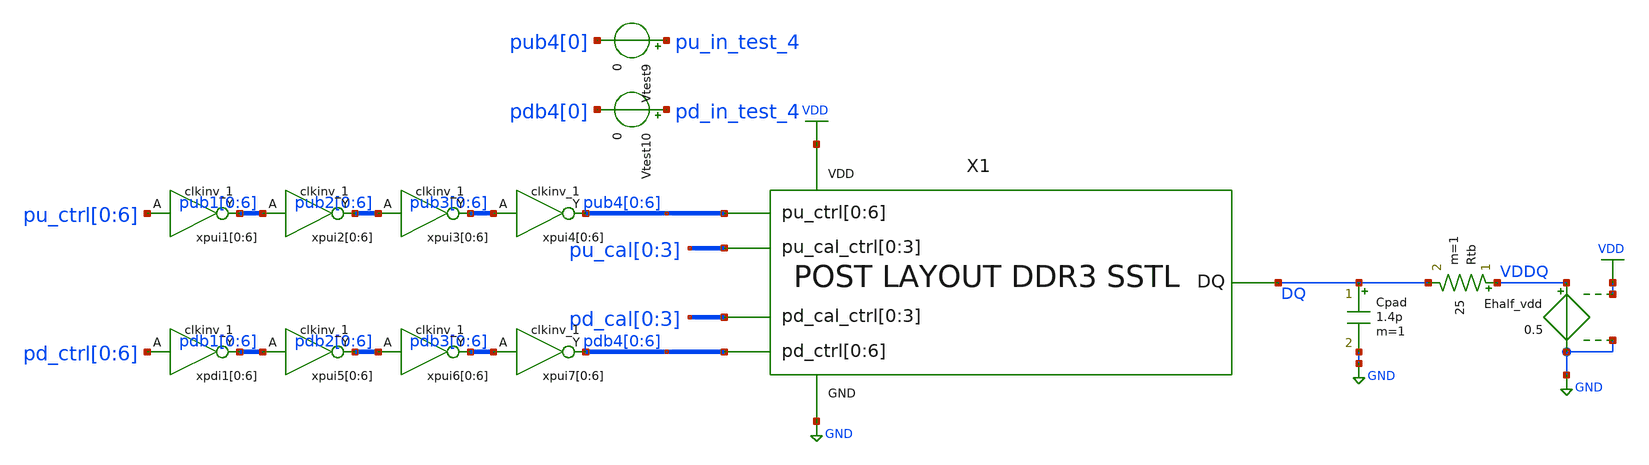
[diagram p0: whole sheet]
** sch_path: schem/post_layout_sstl_slew_tb.sch
* Copyright 2021 Stefan Frederik Schippers
* Licensed under the Apache License, Version 2.0 (the "License");
* you may not use this file except in compliance with the License.
* You may obtain a copy of the License at
* https://www.apache.org/licenses/LICENSE-2.0
* Unless required by applicable law or agreed to in writing, software
* distributed under the License is distributed on an "AS IS" BASIS,
* WITHOUT WARRANTIES OR CONDITIONS OF ANY KIND, either express or implied.
* See the License for the specific language governing permissions and
* limitations under the License.
**.subckt post_layout_sstl_slew_tb
Rtb VDDQ DQ 25 m=1
Cpad DQ GND 1.4p m=1
Ehalf_vdd VDDQ GND VDD GND 0.5
xpui1[0] pu_ctrl[0] GND GND VDD VDD pub1[0] sky130_fd_sc_hd__clkinv_1
xpui1[1] pu_ctrl[1] GND GND VDD VDD pub1[1] sky130_fd_sc_hd__clkinv_1
xpui1[2] pu_ctrl[2] GND GND VDD VDD pub1[2] sky130_fd_sc_hd__clkinv_1
xpui1[3] pu_ctrl[3] GND GND VDD VDD pub1[3] sky130_fd_sc_hd__clkinv_1
xpui1[4] pu_ctrl[4] GND GND VDD VDD pub1[4] sky130_fd_sc_hd__clkinv_1
xpui1[5] pu_ctrl[5] GND GND VDD VDD pub1[5] sky130_fd_sc_hd__clkinv_1
xpui1[6] pu_ctrl[6] GND GND VDD VDD pub1[6] sky130_fd_sc_hd__clkinv_1
xpdi1[0] pd_ctrl[0] GND GND VDD VDD pdb1[0] sky130_fd_sc_hd__clkinv_1
xpdi1[1] pd_ctrl[1] GND GND VDD VDD pdb1[1] sky130_fd_sc_hd__clkinv_1
xpdi1[2] pd_ctrl[2] GND GND VDD VDD pdb1[2] sky130_fd_sc_hd__clkinv_1
xpdi1[3] pd_ctrl[3] GND GND VDD VDD pdb1[3] sky130_fd_sc_hd__clkinv_1
xpdi1[4] pd_ctrl[4] GND GND VDD VDD pdb1[4] sky130_fd_sc_hd__clkinv_1
xpdi1[5] pd_ctrl[5] GND GND VDD VDD pdb1[5] sky130_fd_sc_hd__clkinv_1
xpdi1[6] pd_ctrl[6] GND GND VDD VDD pdb1[6] sky130_fd_sc_hd__clkinv_1
Vtest9 pu_in_test_4 pub4[0] 0
Vtest10 pd_in_test_4 pdb4[0] 0
xpui2[0] pub1[0] GND GND VDD VDD pub2[0] sky130_fd_sc_hd__clkinv_1
xpui2[1] pub1[1] GND GND VDD VDD pub2[1] sky130_fd_sc_hd__clkinv_1
xpui2[2] pub1[2] GND GND VDD VDD pub2[2] sky130_fd_sc_hd__clkinv_1
xpui2[3] pub1[3] GND GND VDD VDD pub2[3] sky130_fd_sc_hd__clkinv_1
xpui2[4] pub1[4] GND GND VDD VDD pub2[4] sky130_fd_sc_hd__clkinv_1
xpui2[5] pub1[5] GND GND VDD VDD pub2[5] sky130_fd_sc_hd__clkinv_1
xpui2[6] pub1[6] GND GND VDD VDD pub2[6] sky130_fd_sc_hd__clkinv_1
xpui3[0] pub2[0] GND GND VDD VDD pub3[0] sky130_fd_sc_hd__clkinv_1
xpui3[1] pub2[1] GND GND VDD VDD pub3[1] sky130_fd_sc_hd__clkinv_1
xpui3[2] pub2[2] GND GND VDD VDD pub3[2] sky130_fd_sc_hd__clkinv_1
xpui3[3] pub2[3] GND GND VDD VDD pub3[3] sky130_fd_sc_hd__clkinv_1
xpui3[4] pub2[4] GND GND VDD VDD pub3[4] sky130_fd_sc_hd__clkinv_1
xpui3[5] pub2[5] GND GND VDD VDD pub3[5] sky130_fd_sc_hd__clkinv_1
xpui3[6] pub2[6] GND GND VDD VDD pub3[6] sky130_fd_sc_hd__clkinv_1
xpui4[0] pub3[0] GND GND VDD VDD pub4[0] sky130_fd_sc_hd__clkinv_1
xpui4[1] pub3[1] GND GND VDD VDD pub4[1] sky130_fd_sc_hd__clkinv_1
xpui4[2] pub3[2] GND GND VDD VDD pub4[2] sky130_fd_sc_hd__clkinv_1
xpui4[3] pub3[3] GND GND VDD VDD pub4[3] sky130_fd_sc_hd__clkinv_1
xpui4[4] pub3[4] GND GND VDD VDD pub4[4] sky130_fd_sc_hd__clkinv_1
xpui4[5] pub3[5] GND GND VDD VDD pub4[5] sky130_fd_sc_hd__clkinv_1
xpui4[6] pub3[6] GND GND VDD VDD pub4[6] sky130_fd_sc_hd__clkinv_1
xpui5[0] pdb1[0] GND GND VDD VDD pdb2[0] sky130_fd_sc_hd__clkinv_1
xpui5[1] pdb1[1] GND GND VDD VDD pdb2[1] sky130_fd_sc_hd__clkinv_1
xpui5[2] pdb1[2] GND GND VDD VDD pdb2[2] sky130_fd_sc_hd__clkinv_1
xpui5[3] pdb1[3] GND GND VDD VDD pdb2[3] sky130_fd_sc_hd__clkinv_1
xpui5[4] pdb1[4] GND GND VDD VDD pdb2[4] sky130_fd_sc_hd__clkinv_1
xpui5[5] pdb1[5] GND GND VDD VDD pdb2[5] sky130_fd_sc_hd__clkinv_1
xpui5[6] pdb1[6] GND GND VDD VDD pdb2[6] sky130_fd_sc_hd__clkinv_1
xpui6[0] pdb2[0] GND GND VDD VDD pdb3[0] sky130_fd_sc_hd__clkinv_1
xpui6[1] pdb2[1] GND GND VDD VDD pdb3[1] sky130_fd_sc_hd__clkinv_1
xpui6[2] pdb2[2] GND GND VDD VDD pdb3[2] sky130_fd_sc_hd__clkinv_1
xpui6[3] pdb2[3] GND GND VDD VDD pdb3[3] sky130_fd_sc_hd__clkinv_1
xpui6[4] pdb2[4] GND GND VDD VDD pdb3[4] sky130_fd_sc_hd__clkinv_1
xpui6[5] pdb2[5] GND GND VDD VDD pdb3[5] sky130_fd_sc_hd__clkinv_1
xpui6[6] pdb2[6] GND GND VDD VDD pdb3[6] sky130_fd_sc_hd__clkinv_1
xpui7[0] pdb3[0] GND GND VDD VDD pdb4[0] sky130_fd_sc_hd__clkinv_1
xpui7[1] pdb3[1] GND GND VDD VDD pdb4[1] sky130_fd_sc_hd__clkinv_1
xpui7[2] pdb3[2] GND GND VDD VDD pdb4[2] sky130_fd_sc_hd__clkinv_1
xpui7[3] pdb3[3] GND GND VDD VDD pdb4[3] sky130_fd_sc_hd__clkinv_1
xpui7[4] pdb3[4] GND GND VDD VDD pdb4[4] sky130_fd_sc_hd__clkinv_1
xpui7[5] pdb3[5] GND GND VDD VDD pdb4[5] sky130_fd_sc_hd__clkinv_1
xpui7[6] pdb3[6] GND GND VDD VDD pdb4[6] sky130_fd_sc_hd__clkinv_1
X1 DQ GND pd_cal[0] pd_cal[1] pd_cal[2] pd_cal[3] pdb4[0] pdb4[1] pdb4[2] pdb4[3] pdb4[4] pdb4[5]
+ pdb4[6] pu_cal[0] pu_cal[1] pu_cal[2] pu_cal[3] pub4[0] pub4[1] pub4[2] pub4[3] pub4[4] pub4[5] pub4[6] VDD
+ SSTL
**** begin user architecture code
 ** Local library links to pdk
.lib ./sky130/libs/SED_process_SED_lib.spice SED_process_SED
.include $::SKYWATER_STDCELLS/sky130_fd_sc_hd.spice
.include ./layout/pex_SSTL.spice

**** end user architecture code
**.ends
.GLOBAL GND
.GLOBAL VDD
**** begin user architecture code


* power voltage
vvdd VDD 0 SED_vdd_SED

** CALIBRATION CONTROL **
* PULLUP
vpu_cal0 pu_cal[0] 0 SED_pucal0_SED
vpu_cal1 pu_cal[1] 0 SED_pucal1_SED
vpu_cal2 pu_cal[2] 0 SED_pucal2_SED
vpu_cal3 pu_cal[3] 0 SED_pucal3_SED
* PULLDOWN
vpd_cal0 pd_cal[0] 0 SED_pdcal0_SED
vpd_cal1 pd_cal[1] 0 SED_pdcal1_SED
vpd_cal2 pd_cal[2] 0 SED_pdcal2_SED
vpd_cal3 pd_cal[3] 0 SED_pdcal3_SED

** LEG ENABLE/DISABLE CONTROL
* PULLUP
*          vlow, vhigh, delay, risetime, falltime, pulsewidth, period, phase
vpu_ctrl0 pu_ctrl[0] 0 0 PULSE 0   SED_puctrl0_SED 1n 10p 10p 5n 10n 0
vpu_ctrl1 pu_ctrl[1] 0 0 PULSE 0   SED_puctrl1_SED 1n 10p 10p 5n 10n 0
vpu_ctrl2 pu_ctrl[2] 0 0 PULSE 0   SED_puctrl2_SED 1n 10p 10p 5n 10n 0
vpu_ctrl3 pu_ctrl[3] 0 0 PULSE 0   SED_puctrl3_SED 1n 10p 10p 5n 10n 0
vpu_ctrl4 pu_ctrl[4] 0 0 PULSE 0   SED_puctrl4_SED 1n 10p 10p 5n 10n 0
vpu_ctrl5 pu_ctrl[5] 0 0 PULSE 0   SED_puctrl5_SED 1n 10p 10p 5n 10n 0
vpu_ctrl6 pu_ctrl[6] 0 0 PULSE 0   SED_puctrl6_SED 1n 10p 10p 5n 10n 0
* PULLDOWN (delay was set to 1.1n for better slew...)
vpd_ctrl0 VDD pd_ctrl[0] 0 PULSE 0 SED_pdctrl0_SED 1n 10p 10p 5n 10n 0
vpd_ctrl1 VDD pd_ctrl[1] 0 PULSE 0 SED_pdctrl1_SED 1n 10p 10p 5n 10n 0
vpd_ctrl2 VDD pd_ctrl[2] 0 PULSE 0 SED_pdctrl2_SED 1n 10p 10p 5n 10n 0
vpd_ctrl3 VDD pd_ctrl[3] 0 PULSE 0 SED_pdctrl3_SED 1n 10p 10p 5n 10n 0
vpd_ctrl4 VDD pd_ctrl[4] 0 PULSE 0 SED_pdctrl4_SED 1n 10p 10p 5n 10n 0
vpd_ctrl5 VDD pd_ctrl[5] 0 PULSE 0 SED_pdctrl5_SED 1n 10p 10p 5n 10n 0
vpd_ctrl6 VDD pd_ctrl[6] 0 PULSE 0 SED_pdctrl6_SED 1n 10p 10p 5n 10n 0

.control
save all
set temp=SED_temp_SED

* RUN SIMULATION
tran 1p 8n
* Measure rise time
meas tran tdiff_rise trig dq val=SED_volac_SED rise=1 targ dq val=SED_vohac_SED rise=1
* Measure fall time
meas tran tdiff_fall trig dq val=SED_vohac_SED fall=1 targ dq val=SED_volac_SED fall=1

* OUTPUT
wrdata ./out/SED_plotName_SED/SED_plotName_SED.txt tdiff_rise tdiff_fall
set hcopydevtype = svg
hardcopy ./out/SED_plotName_SED/SED_plotName_SED.svg dq pu_in_test_4 pd_in_test_4 title 'DQ vs time'

hardcopy ./out/SED_plotName_SED/SED_plotName_SED_DBG.svg   pu_in_test_4   pd_in_test_4
+   "x1.p-leg_6/n_cal_ctrl[0]"  "x1.p-leg_6/n_cal_ctrl[1]"  "x1.p-leg_6/n_cal_ctrl[2]"  "x1.p-leg_6/n_cal_ctrl[3]"

hardcopy ./out/SED_plotName_SED/SED_plotName_SED_DBG2.svg   pu_in_test_4   pd_in_test_4
+   "x1.p-leg_0/n_pu_ctrl"  "x1.n-leg_0/pd_ctrl"



*plot dq pu_in_test_4 pd_in_test_4 x1.v_pu_ctrl_0 x1.v_pd_ctrl_0

.endc


**** end user architecture code
.end
